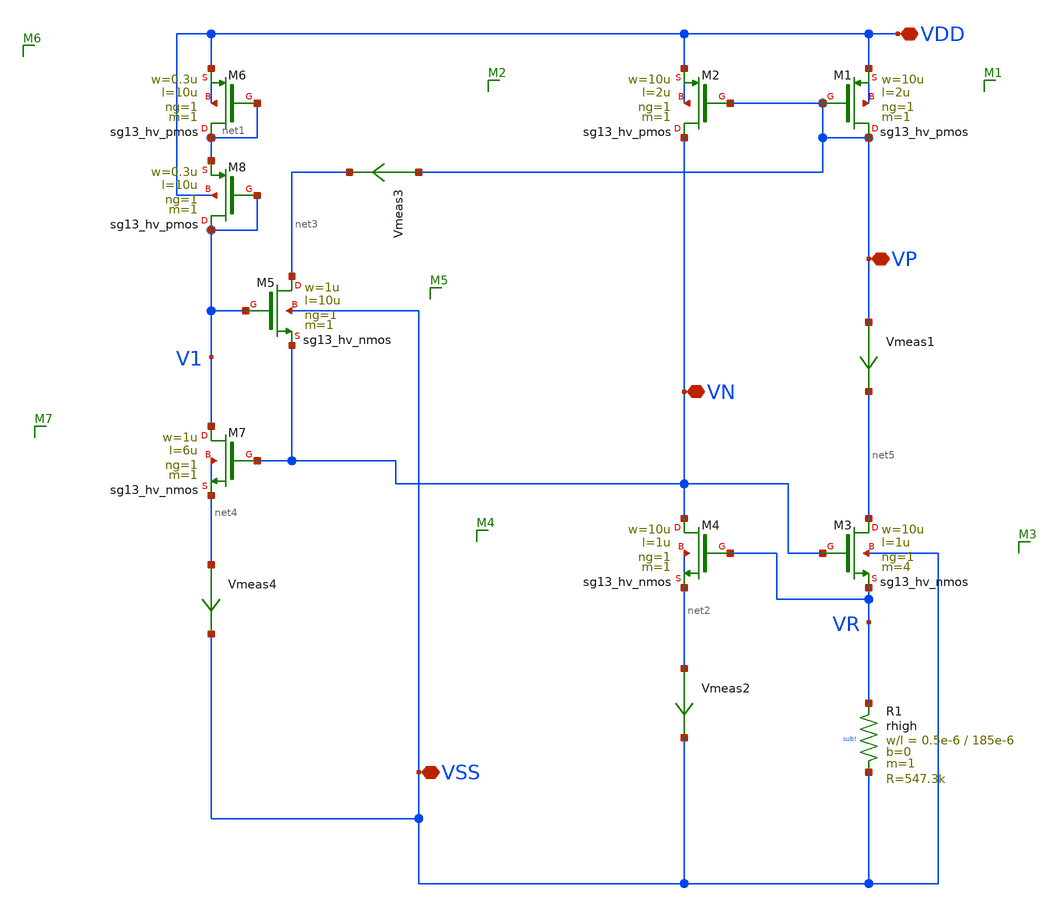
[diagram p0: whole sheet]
** sch_path: dependencies/PMU/PMU-main/schematic/xschem/1u_Ref.sch
**.subckt 1u_Ref VDD VSS VP VN
*.iopin VDD
*.iopin VSS
*.iopin VP
*.iopin VN
XM1 VP VP VDD VDD sg13_hv_pmos w=10u l=2u ng=1 m=1 mm_ok=1
XM2 VN VP VDD VDD sg13_hv_pmos w=10u l=2u ng=1 m=1 mm_ok=1
XM6 net1 net1 VDD VDD sg13_hv_pmos w=0.3u l=10u ng=1 m=1 mm_ok=1
XM7 V1 VN net4 net4 sg13_hv_nmos w=1u l=6u ng=1 m=1 mm_ok=1
XM5 net3 V1 VN VSS sg13_hv_nmos w=1u l=10u ng=1 m=1 mm_ok=1
Vmeas2 net2 VSS 0
.save i(vmeas2)
XM4 VN VR net2 net2 sg13_hv_nmos w=10u l=1u ng=1 m=1 mm_ok=1
XM3 net5 VN VR VSS sg13_hv_nmos w=10u l=1u ng=1 m=4 mm_ok=1
Vmeas1 VP net5 0
.save i(vmeas1)
Vmeas3 VP net3 0
.save i(vmeas3)
Vmeas4 net4 VSS 0
.save i(vmeas4)
XM8 V1 V1 net1 VDD sg13_hv_pmos w=0.3u l=10u ng=1 m=1 mm_ok=1
XR1 VR VSS sub! rhigh w=0.5e-6 l=185e-6 m=1 b=0 mm_ok=1
**.ends
.end
